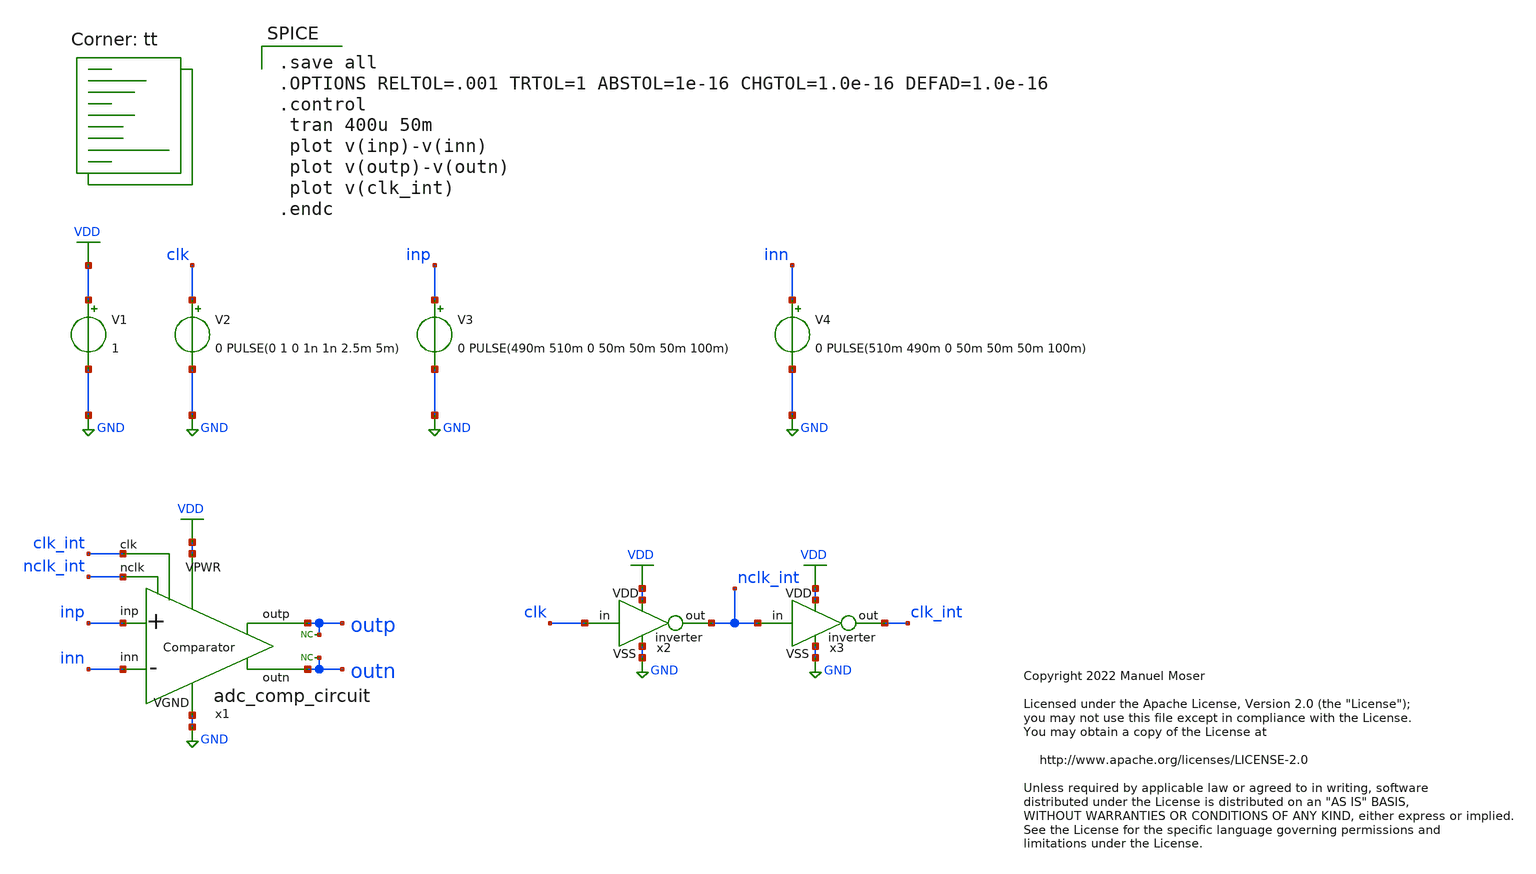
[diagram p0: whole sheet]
** sch_path: xschem/adc_comp_circuit/adc_comp_circuit_tb.sch
* Copyright 2022 Manuel Moser
* Licensed under the Apache License, Version 2.0 (the "License");
**.subckt adc_comp_circuit_tb
V1 VDD GND 1
V2 clk GND 0 PULSE(0 1 0 1n 1n 2.5m 5m)
x2 VDD nclk_int clk GND inverter
x3 VDD clk_int nclk_int GND inverter
V3 inp GND 0 PULSE(490m 510m 0 50m 50m 50m 100m)
V4 inn GND 0 PULSE(510m 490m 0 50m 50m 50m 100m)
* noconn outp
* noconn outn
x1 VDD GND clk_int nclk_int inp inn outp outn adc_comp_circuit
**** begin user architecture code
.lib $::SKYWATER_MODELS/sky130.lib.spice tt

.save all
.OPTIONS RELTOL=.001 TRTOL=1 ABSTOL=1e-16 CHGTOL=1.0e-16 DEFAD=1.0e-16
.control
 tran 400u 50m
 plot v(inp)-v(inn)
 plot v(outp)-v(outn)
 plot v(clk_int)
.endc

**** end user architecture code
**.ends

* expanding   symbol:  /foss/designs/SKY130_SAR-ADC/xschem/inverter/inverter.sym # of pins=4
** sym_path: xschem/inverter/inverter.sym
** sch_path: xschem/inverter/inverter.sch
.subckt inverter VDD out in VSS
*.iopin VDD
*.iopin VSS
*.opin out
*.ipin in
XM1 out in VSS VSS sky130_fd_pr__nfet_01v8 L=0.15 W=0.42 nf=1 ad='int((nf+1)/2) * W/nf * 0.29' as='int((nf+2)/2) * W/nf * 0.29'
+ pd='2*int((nf+1)/2) * (W/nf + 0.29)' ps='2*int((nf+2)/2) * (W/nf + 0.29)' nrd='0.29 / W' nrs='0.29 / W'
+ sa=0 sb=0 sd=0 mult=1 m=1
XM2 out in VDD VDD sky130_fd_pr__pfet_01v8 L=0.15 W=0.42 nf=1 ad='int((nf+1)/2) * W/nf * 0.29' as='int((nf+2)/2) * W/nf * 0.29'
+ pd='2*int((nf+1)/2) * (W/nf + 0.29)' ps='2*int((nf+2)/2) * (W/nf + 0.29)' nrd='0.29 / W' nrs='0.29 / W'
+ sa=0 sb=0 sd=0 mult=1 m=1
.ends


* expanding   symbol:  /foss/designs/SKY130_SAR-ADC/xschem/adc_comp_circuit/adc_comp_circuit.sym #
*+ of pins=8
** sym_path: xschem/adc_comp_circuit.sym
** sch_path: xschem/adc_comp_circuit.sch
.subckt adc_comp_circuit VPWR VGND clk nclk inp inn outp outn
*.iopin VPWR
*.iopin VGND
*.ipin clk
*.ipin nclk
*.ipin inp
*.ipin inn
*.opin outp
*.opin outn
XM3 on inp net1 VGND sky130_fd_pr__nfet_01v8_lvt L=0.15 W=8 nf=4 ad='int((nf+1)/2) * W/nf * 0.29' as='int((nf+2)/2) * W/nf * 0.29'
+ pd='2*int((nf+1)/2) * (W/nf + 0.29)' ps='2*int((nf+2)/2) * (W/nf + 0.29)' nrd='0.29 / W' nrs='0.29 / W'
+ sa=0 sb=0 sd=0 mult=1 m=1
XM4 op inn net1 VGND sky130_fd_pr__nfet_01v8_lvt L=0.15 W=8 nf=4 ad='int((nf+1)/2) * W/nf * 0.29' as='int((nf+2)/2) * W/nf * 0.29'
+ pd='2*int((nf+1)/2) * (W/nf + 0.29)' ps='2*int((nf+2)/2) * (W/nf + 0.29)' nrd='0.29 / W' nrs='0.29 / W'
+ sa=0 sb=0 sd=0 mult=1 m=1
XM5 net1 clk VGND VGND sky130_fd_pr__nfet_01v8 L=0.15 W=4 nf=8 ad='int((nf+1)/2) * W/nf * 0.29' as='int((nf+2)/2) * W/nf * 0.29'
+ pd='2*int((nf+1)/2) * (W/nf + 0.29)' ps='2*int((nf+2)/2) * (W/nf + 0.29)' nrd='0.29 / W' nrs='0.29 / W'
+ sa=0 sb=0 sd=0 mult=1 m=1
XM6 net3 bp VPWR VPWR sky130_fd_pr__pfet_01v8 L=0.15 W=4 nf=2 ad='int((nf+1)/2) * W/nf * 0.29' as='int((nf+2)/2) * W/nf * 0.29'
+ pd='2*int((nf+1)/2) * (W/nf + 0.29)' ps='2*int((nf+2)/2) * (W/nf + 0.29)' nrd='0.29 / W' nrs='0.29 / W'
+ sa=0 sb=0 sd=0 mult=1 m=1
XM7 net2 bn VPWR VPWR sky130_fd_pr__pfet_01v8 L=0.15 W=4 nf=2 ad='int((nf+1)/2) * W/nf * 0.29' as='int((nf+2)/2) * W/nf * 0.29'
+ pd='2*int((nf+1)/2) * (W/nf + 0.29)' ps='2*int((nf+2)/2) * (W/nf + 0.29)' nrd='0.29 / W' nrs='0.29 / W'
+ sa=0 sb=0 sd=0 mult=1 m=1
XM8 bn op net3 VPWR sky130_fd_pr__pfet_01v8 L=0.15 W=4 nf=2 ad='int((nf+1)/2) * W/nf * 0.29' as='int((nf+2)/2) * W/nf * 0.29'
+ pd='2*int((nf+1)/2) * (W/nf + 0.29)' ps='2*int((nf+2)/2) * (W/nf + 0.29)' nrd='0.29 / W' nrs='0.29 / W'
+ sa=0 sb=0 sd=0 mult=1 m=1
XM9 bp on net2 VPWR sky130_fd_pr__pfet_01v8 L=0.15 W=4 nf=2 ad='int((nf+1)/2) * W/nf * 0.29' as='int((nf+2)/2) * W/nf * 0.29'
+ pd='2*int((nf+1)/2) * (W/nf + 0.29)' ps='2*int((nf+2)/2) * (W/nf + 0.29)' nrd='0.29 / W' nrs='0.29 / W'
+ sa=0 sb=0 sd=0 mult=1 m=1
XM10 bn bp VGND VGND sky130_fd_pr__nfet_01v8 L=0.15 W=2 nf=1 ad='int((nf+1)/2) * W/nf * 0.29' as='int((nf+2)/2) * W/nf * 0.29'
+ pd='2*int((nf+1)/2) * (W/nf + 0.29)' ps='2*int((nf+2)/2) * (W/nf + 0.29)' nrd='0.29 / W' nrs='0.29 / W'
+ sa=0 sb=0 sd=0 mult=1 m=1
XM11 bn nclk VGND VGND sky130_fd_pr__nfet_01v8 L=0.15 W=2 nf=1 ad='int((nf+1)/2) * W/nf * 0.29' as='int((nf+2)/2) * W/nf * 0.29'
+ pd='2*int((nf+1)/2) * (W/nf + 0.29)' ps='2*int((nf+2)/2) * (W/nf + 0.29)' nrd='0.29 / W' nrs='0.29 / W'
+ sa=0 sb=0 sd=0 mult=1 m=1
XM12 bp nclk VGND VGND sky130_fd_pr__nfet_01v8 L=0.15 W=2 nf=1 ad='int((nf+1)/2) * W/nf * 0.29' as='int((nf+2)/2) * W/nf * 0.29'
+ pd='2*int((nf+1)/2) * (W/nf + 0.29)' ps='2*int((nf+2)/2) * (W/nf + 0.29)' nrd='0.29 / W' nrs='0.29 / W'
+ sa=0 sb=0 sd=0 mult=1 m=1
XM13 bp bn VGND VGND sky130_fd_pr__nfet_01v8 L=0.15 W=2 nf=1 ad='int((nf+1)/2) * W/nf * 0.29' as='int((nf+2)/2) * W/nf * 0.29'
+ pd='2*int((nf+1)/2) * (W/nf + 0.29)' ps='2*int((nf+2)/2) * (W/nf + 0.29)' nrd='0.29 / W' nrs='0.29 / W'
+ sa=0 sb=0 sd=0 mult=1 m=1
XM2 op clk VPWR VPWR sky130_fd_pr__pfet_01v8 L=0.15 W=2 nf=4 ad='int((nf+1)/2) * W/nf * 0.29' as='int((nf+2)/2) * W/nf * 0.29'
+ pd='2*int((nf+1)/2) * (W/nf + 0.29)' ps='2*int((nf+2)/2) * (W/nf + 0.29)' nrd='0.29 / W' nrs='0.29 / W'
+ sa=0 sb=0 sd=0 mult=1 m=1
XM1 on clk VPWR VPWR sky130_fd_pr__pfet_01v8 L=0.15 W=2 nf=4 ad='int((nf+1)/2) * W/nf * 0.29' as='int((nf+2)/2) * W/nf * 0.29'
+ pd='2*int((nf+1)/2) * (W/nf + 0.29)' ps='2*int((nf+2)/2) * (W/nf + 0.29)' nrd='0.29 / W' nrs='0.29 / W'
+ sa=0 sb=0 sd=0 mult=1 m=1
x1 VPWR VGND bp outp adc_comp_buffer
x2 VPWR VGND bn outn adc_comp_buffer
x3 VGND VGND on VGND VGND adc_noise_decoup_cell2
x4 VGND VGND op VGND VGND adc_noise_decoup_cell2
.ends


* expanding   symbol:  adc_comp_buffer.sym # of pins=4
** sym_path: xschem/adc_comp_buffer.sym
** sch_path: xschem/adc_comp_buffer.sch
.subckt adc_comp_buffer VDD VSS in out
*.iopin VDD
*.iopin VSS
*.ipin in
*.opin out
XM5 net1 in VSS VSS sky130_fd_pr__nfet_01v8 L=0.15 W=0.5 nf=1 ad='int((nf+1)/2) * W/nf * 0.29' as='int((nf+2)/2) * W/nf * 0.29'
+ pd='2*int((nf+1)/2) * (W/nf + 0.29)' ps='2*int((nf+2)/2) * (W/nf + 0.29)' nrd='0.29 / W' nrs='0.29 / W'
+ sa=0 sb=0 sd=0 mult=1 m=1
XM1 net1 in VDD VDD sky130_fd_pr__pfet_01v8 L=0.15 W=1 nf=1 ad='int((nf+1)/2) * W/nf * 0.29' as='int((nf+2)/2) * W/nf * 0.29'
+ pd='2*int((nf+1)/2) * (W/nf + 0.29)' ps='2*int((nf+2)/2) * (W/nf + 0.29)' nrd='0.29 / W' nrs='0.29 / W'
+ sa=0 sb=0 sd=0 mult=1 m=1
XM2 out net1 VDD VDD sky130_fd_pr__pfet_01v8 L=0.15 W=2 nf=2 ad='int((nf+1)/2) * W/nf * 0.29' as='int((nf+2)/2) * W/nf * 0.29'
+ pd='2*int((nf+1)/2) * (W/nf + 0.29)' ps='2*int((nf+2)/2) * (W/nf + 0.29)' nrd='0.29 / W' nrs='0.29 / W'
+ sa=0 sb=0 sd=0 mult=1 m=1
XM6 out net1 VSS VSS sky130_fd_pr__nfet_01v8 L=0.15 W=1 nf=2 ad='int((nf+1)/2) * W/nf * 0.29' as='int((nf+2)/2) * W/nf * 0.29'
+ pd='2*int((nf+1)/2) * (W/nf + 0.29)' ps='2*int((nf+2)/2) * (W/nf + 0.29)' nrd='0.29 / W' nrs='0.29 / W'
+ sa=0 sb=0 sd=0 mult=1 m=1
.ends


* expanding   symbol:  adc_noise_decoup_cell2.sym # of pins=5
** sym_path: xschem/adc_noise_decoup_cell2.sym
** sch_path: xschem/adc_noise_decoup_cell2.sch
.subckt adc_noise_decoup_cell2 mimcap_top mimcap_bot nmoscap_top nmoscap_bot pwell
*.iopin nmoscap_top
*.iopin mimcap_top
*.iopin mimcap_bot
*.iopin nmoscap_bot
*.iopin pwell
XC1 mimcap_top mimcap_bot sky130_fd_pr__cap_mim_m3_1 W=18.9 L=5.1 MF=1 m=1
XC2 nmoscap_top nmoscap_bot pwell sky130_fd_pr__cap_var_lvt W=18.4 L=3.9 VM=1 m=1
.ends

.GLOBAL GND
.GLOBAL VDD
.end
